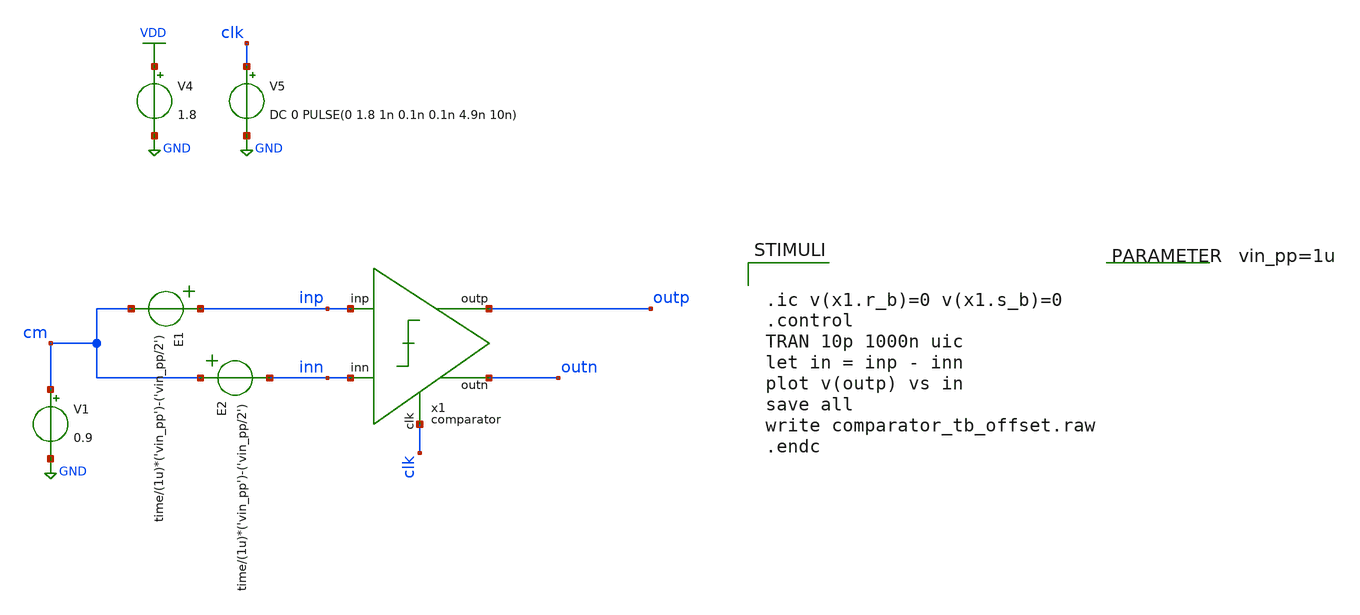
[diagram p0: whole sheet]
** sch_path: verification/schematic/comparator_tb_offset.sch
**.subckt comparator_tb_offset
x1 inp inn outp clk outn VDD GND comparator
V1 cm GND 0.9
V4 VDD GND 1.8
V5 clk GND DC 0 PULSE(0 1.8 1n 0.1n 0.1n 4.9n 10n)
.param vin_pp=1u
E1 inp cm VOL=' time/(1u)*('vin_pp')-('vin_pp/2') '
E2 cm inn VOL=' time/(1u)*('vin_pp')-('vin_pp/2') '
**** begin user architecture code

** opencircuitdesign pdks install
.lib /farmshare/home/classes/ee/372/PDKs/open_pdks_1.0.310/sky130/sky130A/libs.tech/ngspice/sky130.lib.spice tt
.inc /farmshare/home/classes/ee/372/PDKs/open_pdks_1.0.310/sky130/sky130A/libs.ref/sky130_fd_sc_hd/spice/sky130_fd_sc_hd.spice



.ic v(x1.r_b)=0 v(x1.s_b)=0
.control
TRAN 10p 1000n uic
let in = inp - inn
plot v(outp) vs in
save all
write comparator_tb_offset.raw
.endc



**** end user architecture code
**.ends
.GLOBAL GND
.GLOBAL VDD
.end
